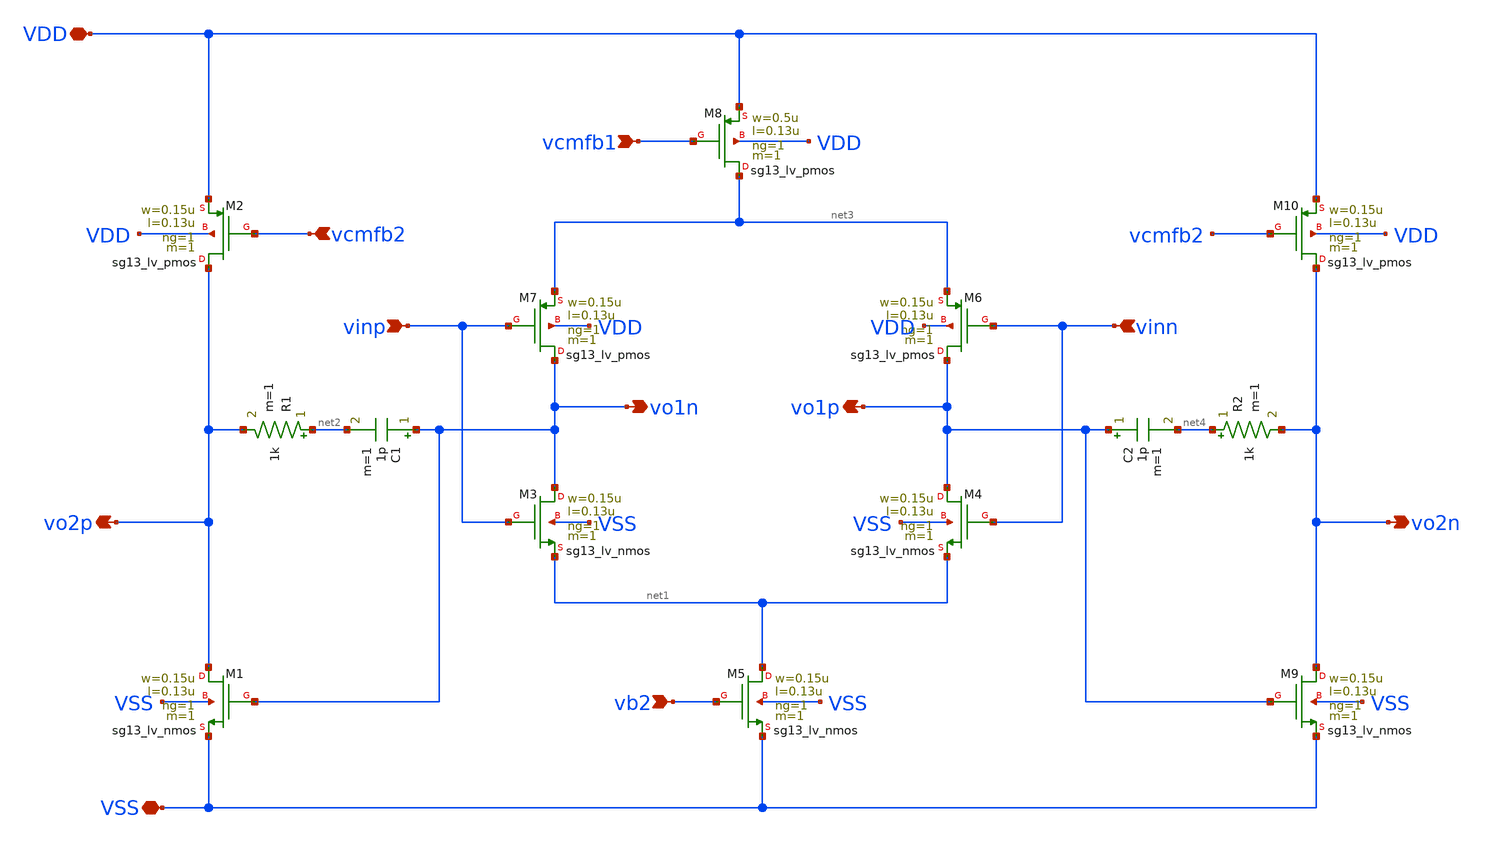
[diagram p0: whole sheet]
** sch_path: analog-db/drawings/bio-afe-01-YuPinHsu-reconfigable-SRMC/SRMC-core-amp.sch
* Copyright 2026 MacAnalog Research Group
**.subckt SRMC-core-amp VDD VSS vinn vinp vo2p vo2n vcmfb2 vcmfb1 vb2 vo1n vo1p
*.iopin VDD
*.iopin VSS
*.ipin vinn
*.ipin vinp
*.opin vo2p
*.opin vo2n
*.ipin vcmfb2
*.ipin vcmfb1
*.ipin vb2
*.opin vo1n
*.opin vo1p
XM1 vo2p vo1n VSS VSS sg13_lv_nmos w=0.15u l=0.13u ng=1 m=1 mm_ok=1
XM2 vo2p vcmfb2 VDD VDD sg13_lv_pmos w=0.15u l=0.13u ng=1 m=1 mm_ok=1
C1 vo1n net2 1p m=1
R1 net2 vo2p 1k m=1
XM3 vo1n vinp net1 VSS sg13_lv_nmos w=0.15u l=0.13u ng=1 m=1 mm_ok=1
XM4 vo1p vinn net1 VSS sg13_lv_nmos w=0.15u l=0.13u ng=1 m=1 mm_ok=1
XM5 net1 vb2 VSS VSS sg13_lv_nmos w=0.15u l=0.13u ng=1 m=1 mm_ok=1
XM6 vo1p vinn net3 VDD sg13_lv_pmos w=0.15u l=0.13u ng=1 m=1 mm_ok=1
XM7 vo1n vinp net3 VDD sg13_lv_pmos w=0.15u l=0.13u ng=1 m=1 mm_ok=1
XM8 net3 vcmfb1 VDD VDD sg13_lv_pmos w=0.5u l=0.13u ng=1 m=1 mm_ok=1
XM9 vo2n vo1p VSS VSS sg13_lv_nmos w=0.15u l=0.13u ng=1 m=1 mm_ok=1
XM10 vo2n vcmfb2 VDD VDD sg13_lv_pmos w=0.15u l=0.13u ng=1 m=1 mm_ok=1
C2 vo1p net4 1p m=1
R2 net4 vo2n 1k m=1
**.ends
.end
